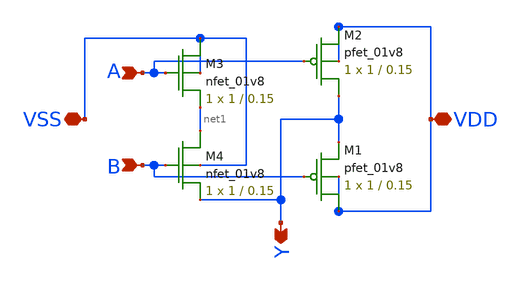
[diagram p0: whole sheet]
** sch_path: nand2.sch
**.subckt nand2 VDD VSS A Y B
*.iopin VDD
*.iopin VSS
*.ipin A
*.opin Y
*.ipin B
XM2 Y A VDD VDD sky130_fd_pr__pfet_01v8 L=0.15 W=1 nf=1 ad='int((nf+1)/2) * W/nf * 0.29' as='int((nf+2)/2) * W/nf * 0.29'
+ pd='2*int((nf+1)/2) * (W/nf + 0.29)' ps='2*int((nf+2)/2) * (W/nf + 0.29)' nrd='0.29 / W' nrs='0.29 / W'
+ sa=0 sb=0 sd=0 mult=1 m=1
XM1 VDD B Y VDD sky130_fd_pr__pfet_01v8 L=0.15 W=1 nf=1 ad='int((nf+1)/2) * W/nf * 0.29' as='int((nf+2)/2) * W/nf * 0.29'
+ pd='2*int((nf+1)/2) * (W/nf + 0.29)' ps='2*int((nf+2)/2) * (W/nf + 0.29)' nrd='0.29 / W' nrs='0.29 / W'
+ sa=0 sb=0 sd=0 mult=1 m=1
XM3 VSS A net1 VSS sky130_fd_pr__nfet_01v8 L=0.15 W=1 nf=1 ad='int((nf+1)/2) * W/nf * 0.29' as='int((nf+2)/2) * W/nf * 0.29'
+ pd='2*int((nf+1)/2) * (W/nf + 0.29)' ps='2*int((nf+2)/2) * (W/nf + 0.29)' nrd='0.29 / W' nrs='0.29 / W'
+ sa=0 sb=0 sd=0 mult=1 m=1
XM4 net1 B Y VSS sky130_fd_pr__nfet_01v8 L=0.15 W=1 nf=1 ad='int((nf+1)/2) * W/nf * 0.29' as='int((nf+2)/2) * W/nf * 0.29'
+ pd='2*int((nf+1)/2) * (W/nf + 0.29)' ps='2*int((nf+2)/2) * (W/nf + 0.29)' nrd='0.29 / W' nrs='0.29 / W'
+ sa=0 sb=0 sd=0 mult=1 m=1
**** begin user architecture code
sym_pins="A B Y VDD VSS"




**** end user architecture code
**.ends
.end
